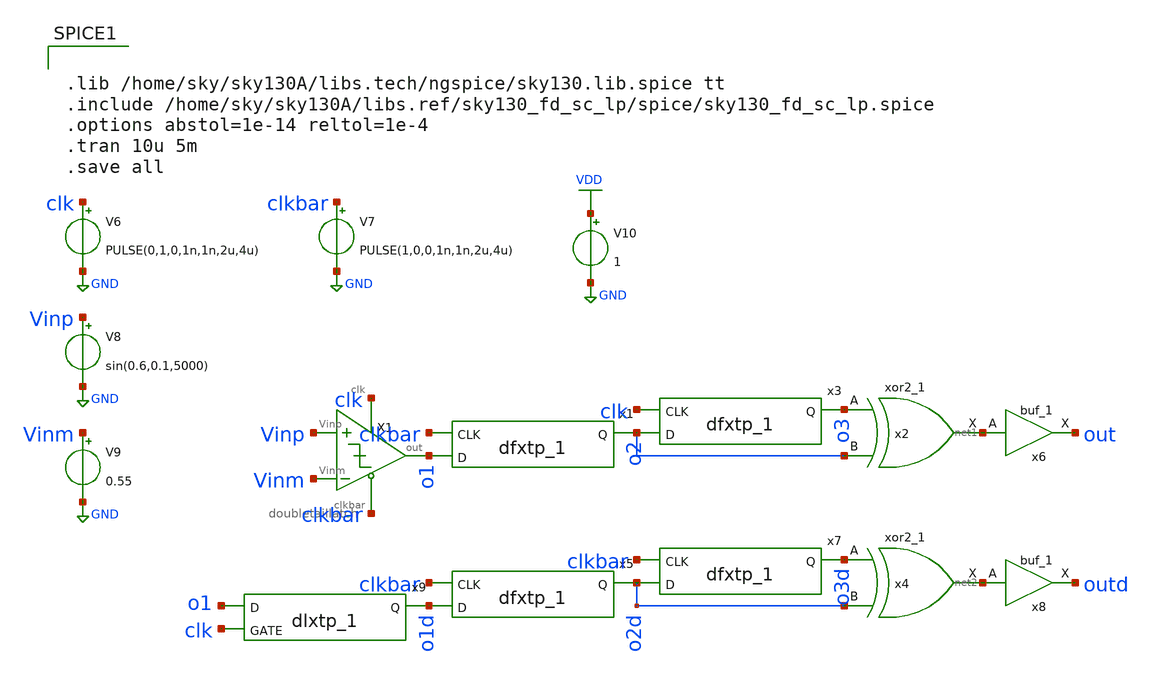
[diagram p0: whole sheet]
** sch_path: xschem/comparator/dlatch_comp_tb.sch
**.subckt dlatch_comp_tb
X1 Vinp Vinm o1 clk clkbar doubletaillatch
V6 clk GND PULSE(0,1,0,1n,1n,2u,4u)
V7 clkbar GND PULSE(1,0,0,1n,1n,2u,4u)
V8 Vinp GND sin(0.6,0.1,5000)
V9 Vinm GND 0.55
V10 VDD GND 1
x2 o3 o2 GND GND VDD VDD net1 sky130_fd_sc_lp__xor2_1
x1 clkbar o1 GND GND VDD VDD o2 sky130_fd_sc_lp__dfxtp_1
x3 clk o2 GND GND VDD VDD o3 sky130_fd_sc_lp__dfxtp_1
x6 net1 GND GND VDD VDD out sky130_fd_sc_lp__buf_1
x4 o3d o2d GND GND VDD VDD net2 sky130_fd_sc_lp__xor2_1
x5 clkbar o1d GND GND VDD VDD o2d sky130_fd_sc_lp__dfxtp_1
x7 clkbar o2d GND GND VDD VDD o3d sky130_fd_sc_lp__dfxtp_1
x8 net2 GND GND VDD VDD outd sky130_fd_sc_lp__buf_1
x9 o1 clk gnd gnd vdd vdd o1d sky130_fd_sc_lp__dlxtp_1
**** begin user architecture code


.lib /home/sky/sky130A/libs.tech/ngspice/sky130.lib.spice tt
.include /home/sky/sky130A/libs.ref/sky130_fd_sc_lp/spice/sky130_fd_sc_lp.spice
.options abstol=1e-14 reltol=1e-4
.tran 10u 5m
.save all


**** end user architecture code
**.ends

* expanding   symbol:  comparator/doubletaillatch.sym # of pins=5
** sym_path: xschem/comparator/doubletaillatch.sym
** sch_path: xschem/comparator/doubletaillatch.sch
.subckt doubletaillatch Vinp Vinm out clk clkbar
*.ipin clkbar
*.opin out
*.ipin Vinp
*.ipin Vinm
*.ipin clk
XM3 net6 out VDD VDD sky130_fd_pr__pfet_01v8 L=1 W=4 nf=1 ad='int((nf+1)/2) * W/nf * 0.29' as='int((nf+2)/2) * W/nf * 0.29'
+ pd='2*int((nf+1)/2) * (W/nf + 0.29)' ps='2*int((nf+2)/2) * (W/nf + 0.29)' nrd='0.29 / W' nrs='0.29 / W'
+ sa=0 sb=0 sd=0 mult=1 m=1
XM4 VDD net1 net7 VDD sky130_fd_pr__pfet_01v8 L=1 W=4 nf=1 ad='int((nf+1)/2) * W/nf * 0.29' as='int((nf+2)/2) * W/nf * 0.29'
+ pd='2*int((nf+1)/2) * (W/nf + 0.29)' ps='2*int((nf+2)/2) * (W/nf + 0.29)' nrd='0.29 / W' nrs='0.29 / W'
+ sa=0 sb=0 sd=0 mult=1 m=1
XM5 net7 net3 out VDD sky130_fd_pr__pfet_01v8 L=1 W=4 nf=1 ad='int((nf+1)/2) * W/nf * 0.29' as='int((nf+2)/2) * W/nf * 0.29'
+ pd='2*int((nf+1)/2) * (W/nf + 0.29)' ps='2*int((nf+2)/2) * (W/nf + 0.29)' nrd='0.29 / W' nrs='0.29 / W'
+ sa=0 sb=0 sd=0 mult=1 m=1
XM6 net1 net4 net6 VDD sky130_fd_pr__pfet_01v8 L=1 W=4 nf=1 ad='int((nf+1)/2) * W/nf * 0.29' as='int((nf+2)/2) * W/nf * 0.29'
+ pd='2*int((nf+1)/2) * (W/nf + 0.29)' ps='2*int((nf+2)/2) * (W/nf + 0.29)' nrd='0.29 / W' nrs='0.29 / W'
+ sa=0 sb=0 sd=0 mult=1 m=1
XM7 out clkbar GND GND sky130_fd_pr__nfet_01v8 L=1 W=2 nf=1 ad='int((nf+1)/2) * W/nf * 0.29' as='int((nf+2)/2) * W/nf * 0.29'
+ pd='2*int((nf+1)/2) * (W/nf + 0.29)' ps='2*int((nf+2)/2) * (W/nf + 0.29)' nrd='0.29 / W' nrs='0.29 / W'
+ sa=0 sb=0 sd=0 mult=1 m=1
XM8 GND net1 out GND sky130_fd_pr__nfet_01v8 L=1 W=2 nf=1 ad='int((nf+1)/2) * W/nf * 0.29' as='int((nf+2)/2) * W/nf * 0.29'
+ pd='2*int((nf+1)/2) * (W/nf + 0.29)' ps='2*int((nf+2)/2) * (W/nf + 0.29)' nrd='0.29 / W' nrs='0.29 / W'
+ sa=0 sb=0 sd=0 mult=1 m=1
XM9 net1 out GND GND sky130_fd_pr__nfet_01v8 L=1 W=2 nf=1 ad='int((nf+1)/2) * W/nf * 0.29' as='int((nf+2)/2) * W/nf * 0.29'
+ pd='2*int((nf+1)/2) * (W/nf + 0.29)' ps='2*int((nf+2)/2) * (W/nf + 0.29)' nrd='0.29 / W' nrs='0.29 / W'
+ sa=0 sb=0 sd=0 mult=1 m=1
XM10 GND clkbar net1 GND sky130_fd_pr__nfet_01v8 L=1 W=2 nf=1 ad='int((nf+1)/2) * W/nf * 0.29' as='int((nf+2)/2) * W/nf * 0.29'
+ pd='2*int((nf+1)/2) * (W/nf + 0.29)' ps='2*int((nf+2)/2) * (W/nf + 0.29)' nrd='0.29 / W' nrs='0.29 / W'
+ sa=0 sb=0 sd=0 mult=1 m=1
XM11 net4 clk VDD VDD sky130_fd_pr__pfet_01v8 L=1 W=4 nf=1 ad='int((nf+1)/2) * W/nf * 0.29' as='int((nf+2)/2) * W/nf * 0.29'
+ pd='2*int((nf+1)/2) * (W/nf + 0.29)' ps='2*int((nf+2)/2) * (W/nf + 0.29)' nrd='0.29 / W' nrs='0.29 / W'
+ sa=0 sb=0 sd=0 mult=1 m=1
XM12 VDD clk net3 VDD sky130_fd_pr__pfet_01v8 L=1 W=4 nf=1 ad='int((nf+1)/2) * W/nf * 0.29' as='int((nf+2)/2) * W/nf * 0.29'
+ pd='2*int((nf+1)/2) * (W/nf + 0.29)' ps='2*int((nf+2)/2) * (W/nf + 0.29)' nrd='0.29 / W' nrs='0.29 / W'
+ sa=0 sb=0 sd=0 mult=1 m=1
XM13 net4 Vinm net2 GND sky130_fd_pr__nfet_01v8 L=1 W=2 nf=1 ad='int((nf+1)/2) * W/nf * 0.29' as='int((nf+2)/2) * W/nf * 0.29'
+ pd='2*int((nf+1)/2) * (W/nf + 0.29)' ps='2*int((nf+2)/2) * (W/nf + 0.29)' nrd='0.29 / W' nrs='0.29 / W'
+ sa=0 sb=0 sd=0 mult=1 m=1
XM14 net2 Vinp net3 GND sky130_fd_pr__nfet_01v8 L=1 W=2 nf=1 ad='int((nf+1)/2) * W/nf * 0.29' as='int((nf+2)/2) * W/nf * 0.29'
+ pd='2*int((nf+1)/2) * (W/nf + 0.29)' ps='2*int((nf+2)/2) * (W/nf + 0.29)' nrd='0.29 / W' nrs='0.29 / W'
+ sa=0 sb=0 sd=0 mult=1 m=1
XM15 net2 clk net5 GND sky130_fd_pr__nfet_01v8 L=1 W=2 nf=1 ad='int((nf+1)/2) * W/nf * 0.29' as='int((nf+2)/2) * W/nf * 0.29'
+ pd='2*int((nf+1)/2) * (W/nf + 0.29)' ps='2*int((nf+2)/2) * (W/nf + 0.29)' nrd='0.29 / W' nrs='0.29 / W'
+ sa=0 sb=0 sd=0 mult=1 m=1
XM16 net5 clkbar GND GND sky130_fd_pr__nfet_01v8 L=1 W=2 nf=1 ad='int((nf+1)/2) * W/nf * 0.29' as='int((nf+2)/2) * W/nf * 0.29'
+ pd='2*int((nf+1)/2) * (W/nf + 0.29)' ps='2*int((nf+2)/2) * (W/nf + 0.29)' nrd='0.29 / W' nrs='0.29 / W'
+ sa=0 sb=0 sd=0 mult=1 m=1
XC2 net5 GND sky130_fd_pr__cap_mim_m3_1 W=10 L=10 MF=1 m=1
XC1 net4 GND sky130_fd_pr__cap_mim_m3_1 W=1 L=1 MF=1 m=1
XC3 net3 GND sky130_fd_pr__cap_mim_m3_1 W=1 L=1 MF=1 m=1
.ends

.GLOBAL VDD
.GLOBAL GND
.end
